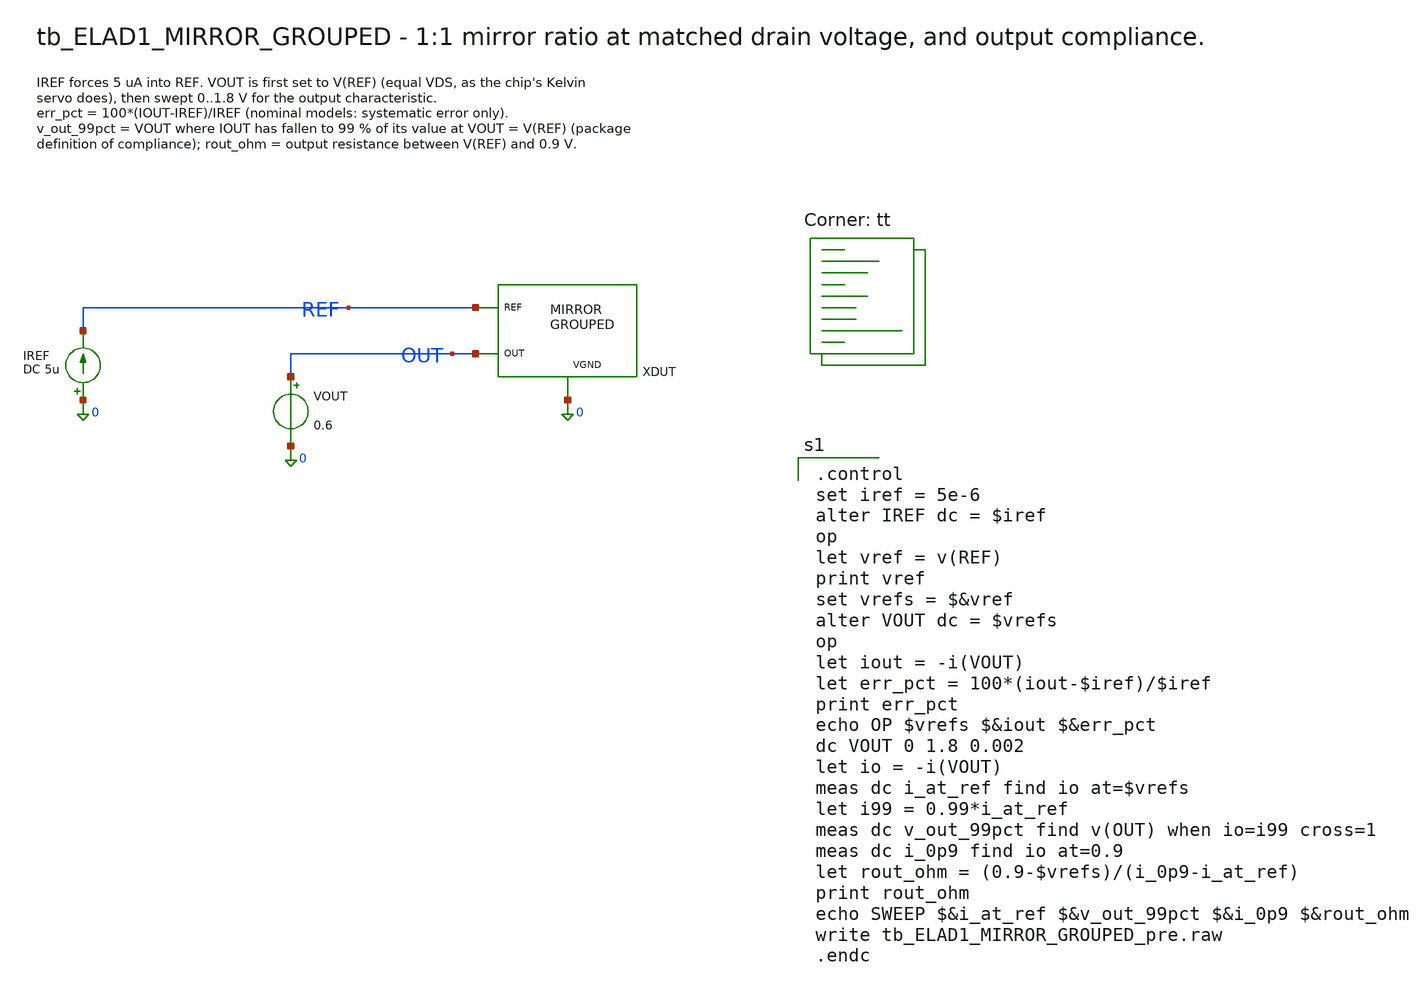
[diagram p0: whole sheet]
** sch_path: cells/ELAD1_MIRROR_GROUPED/schematic/tb_ELAD1_MIRROR_GROUPED.sch
**.subckt tb_ELAD1_MIRROR_GROUPED
XDUT REF OUT 0 ELAD1_MIRROR_GROUPED
VOUT OUT 0 0.6
IREF 0 REF DC 5u
**** begin user architecture code

.control
set iref = 5e-6
alter IREF dc = $iref
op
let vref = v(REF)
print vref
set vrefs = $&vref
alter VOUT dc = $vrefs
op
let iout = -i(VOUT)
let err_pct = 100*(iout-$iref)/$iref
print err_pct
echo OP $vrefs $&iout $&err_pct
dc VOUT 0 1.8 0.002
let io = -i(VOUT)
meas dc i_at_ref find io at=$vrefs
let i99 = 0.99*i_at_ref
meas dc v_out_99pct find v(OUT) when io=i99 cross=1
meas dc i_0p9 find io at=0.9
let rout_ohm = (0.9-$vrefs)/(i_0p9-i_at_ref)
print rout_ohm
echo SWEEP $&i_at_ref $&v_out_99pct $&i_0p9 $&rout_ohm
write tb_ELAD1_MIRROR_GROUPED_pre.raw
.endc

.lib $::SKYWATER_MODELS/sky130.lib.spice tt
**** end user architecture code
**.ends

* expanding   symbol:  ELAD1_MIRROR_GROUPED.sym # of pins=3
** sym_path: cells/ELAD1_MIRROR_GROUPED/schematic/ELAD1_MIRROR_GROUPED.sym
** sch_path: cells/ELAD1_MIRROR_GROUPED/schematic/ELAD1_MIRROR_GROUPED.sch
.subckt ELAD1_MIRROR_GROUPED REF OUT VGND
*.iopin REF
*.iopin OUT
*.iopin VGND
XM1 REF REF VGND VGND sky130_fd_pr__nfet_01v8 L=1 W=8 nf=1 ad='int((1 + 1)/2) * 8 / 1 * 0.29' as='int((1 + 2)/2) * 8 / 1 * 0.29'
+ pd='2*int((1 + 1)/2) * (8 / 1 + 0.29)' ps='2*int((1 + 2)/2) * (8 / 1 + 0.29)' nrd='0.29 / 8 ' nrs='0.29 / 8 '
+ sa=0 sb=0 sd=0 mult=1 m=1
XM2 OUT REF VGND VGND sky130_fd_pr__nfet_01v8 L=1 W=8 nf=1 ad='int((1 + 1)/2) * 8 / 1 * 0.29' as='int((1 + 2)/2) * 8 / 1 * 0.29'
+ pd='2*int((1 + 1)/2) * (8 / 1 + 0.29)' ps='2*int((1 + 2)/2) * (8 / 1 + 0.29)' nrd='0.29 / 8 ' nrs='0.29 / 8 '
+ sa=0 sb=0 sd=0 mult=1 m=1
XM3 VGND VGND VGND VGND sky130_fd_pr__nfet_01v8 L=1 W=8 nf=1 ad='int((1 + 1)/2) * 8 / 1 * 0.29' as='int((1 + 2)/2) * 8 / 1 * 0.29'
+ pd='2*int((1 + 1)/2) * (8 / 1 + 0.29)' ps='2*int((1 + 2)/2) * (8 / 1 + 0.29)' nrd='0.29 / 8 ' nrs='0.29 / 8 '
+ sa=0 sb=0 sd=0 mult=1 m=1
.ends

.end
